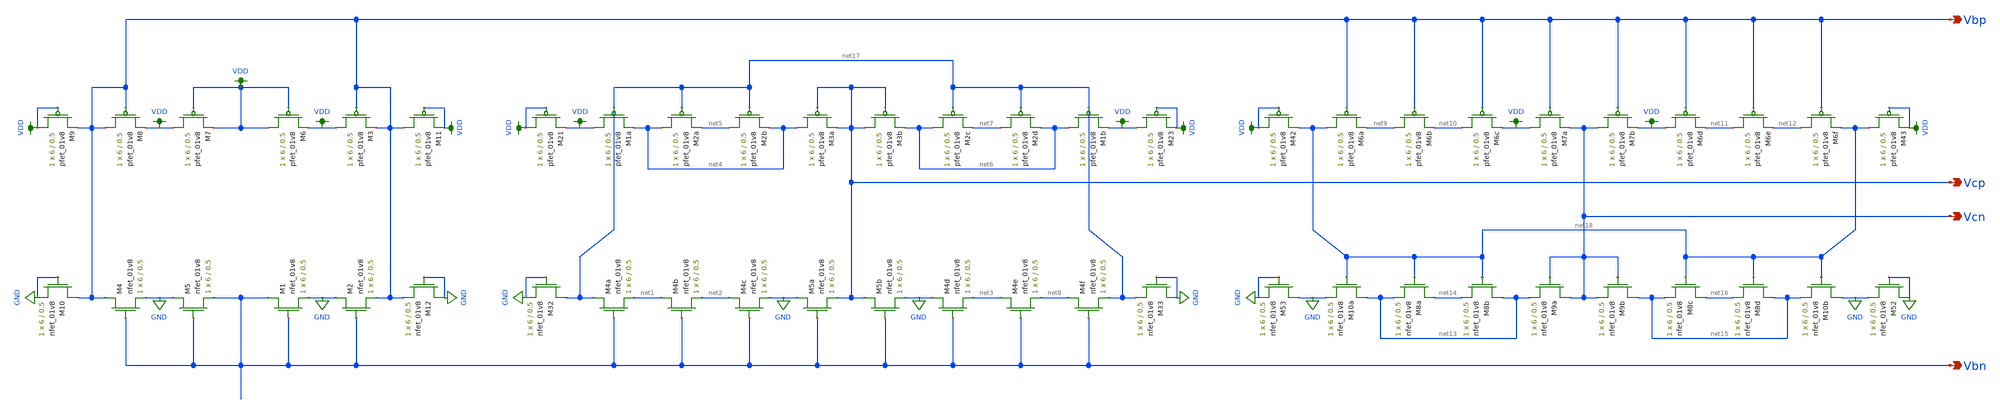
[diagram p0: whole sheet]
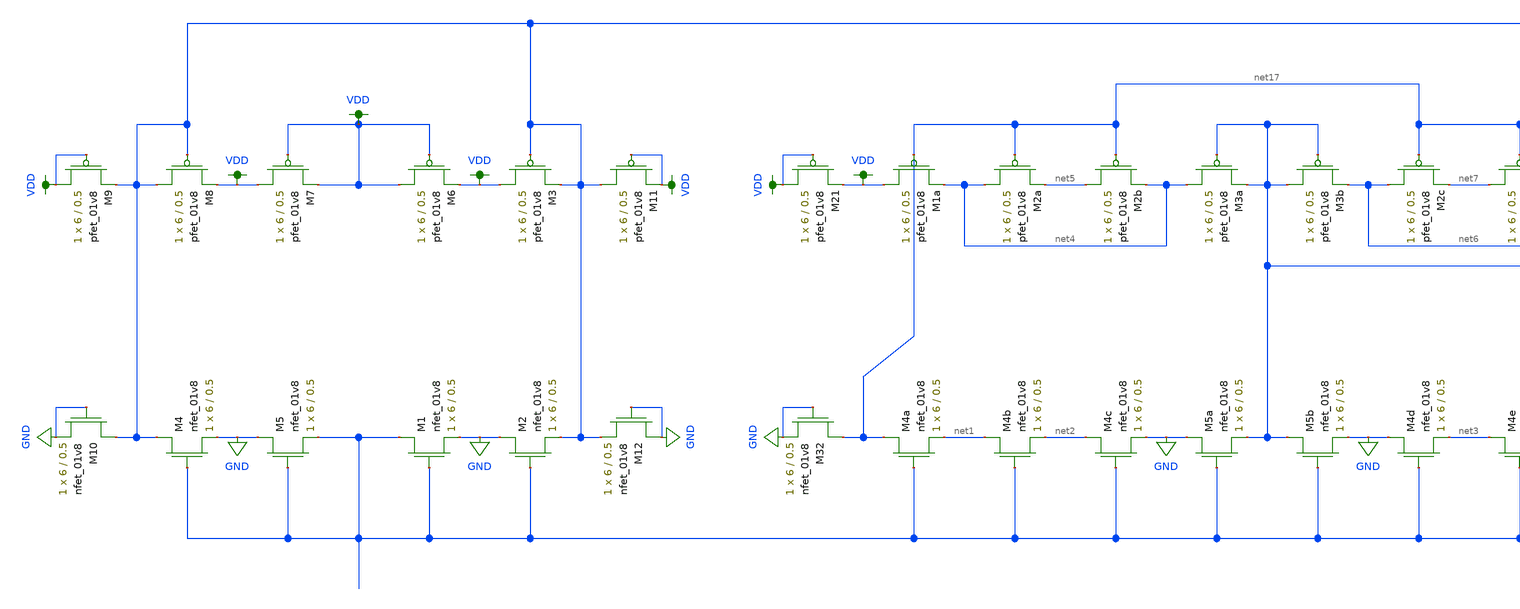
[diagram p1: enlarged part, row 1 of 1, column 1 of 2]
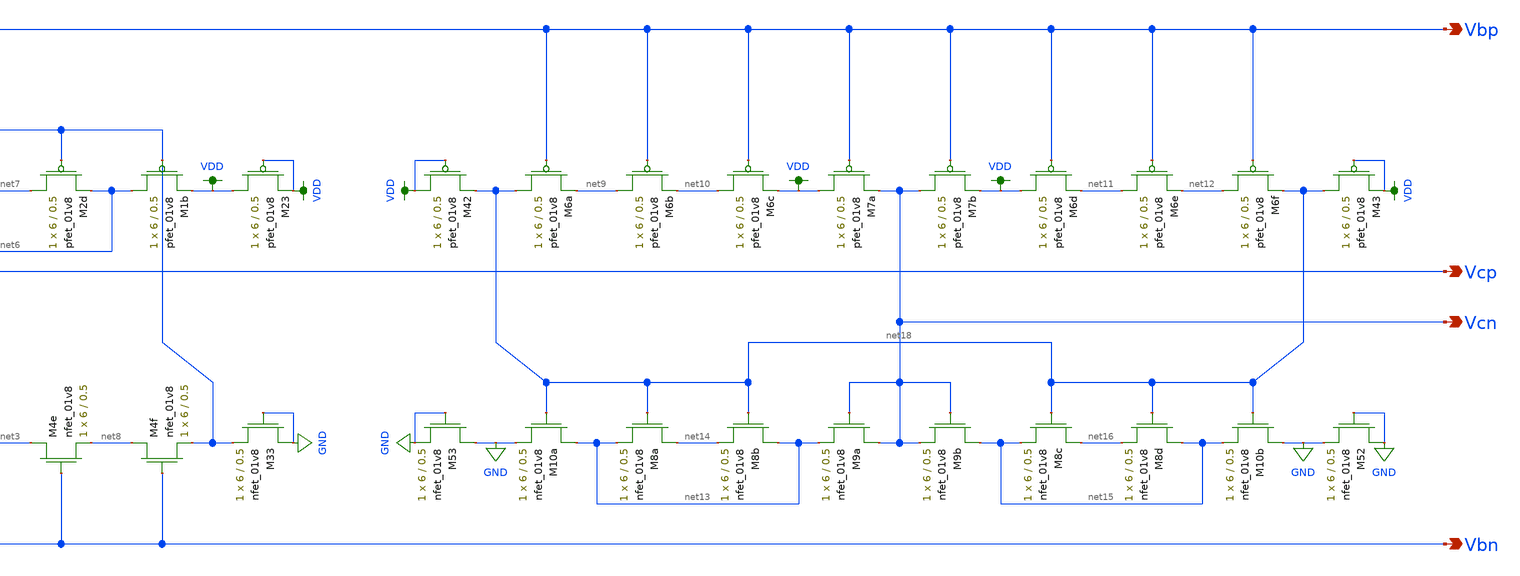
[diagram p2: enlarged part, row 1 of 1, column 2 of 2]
** sch_path: mini3/schem/bias_lvs.sch
**.subckt bias_lvs Vbn Vcn Vcp Vbp
*.opin Vbn
*.opin Vcn
*.opin Vcp
*.opin Vbp
XM4a net17 Vbn net1 GND sky130_fd_pr__nfet_01v8 L=0.5 W=6 nf=1 ad='int((nf+1)/2) * W/nf * 0.29' as='int((nf+2)/2) * W/nf * 0.29'
+ pd='2*int((nf+1)/2) * (W/nf + 0.29)' ps='2*int((nf+2)/2) * (W/nf + 0.29)' nrd='0.29 / W' nrs='0.29 / W'
+ sa=0 sb=0 sd=0 mult=1 m=1
XM4b net1 Vbn net2 GND sky130_fd_pr__nfet_01v8 L=0.5 W=6 nf=1 ad='int((nf+1)/2) * W/nf * 0.29' as='int((nf+2)/2) * W/nf * 0.29'
+ pd='2*int((nf+1)/2) * (W/nf + 0.29)' ps='2*int((nf+2)/2) * (W/nf + 0.29)' nrd='0.29 / W' nrs='0.29 / W'
+ sa=0 sb=0 sd=0 mult=1 m=1
XM4c net2 Vbn GND GND sky130_fd_pr__nfet_01v8 L=0.5 W=6 nf=1 ad='int((nf+1)/2) * W/nf * 0.29' as='int((nf+2)/2) * W/nf * 0.29'
+ pd='2*int((nf+1)/2) * (W/nf + 0.29)' ps='2*int((nf+2)/2) * (W/nf + 0.29)' nrd='0.29 / W' nrs='0.29 / W'
+ sa=0 sb=0 sd=0 mult=1 m=1
XM5a GND Vbn Vcp GND sky130_fd_pr__nfet_01v8 L=0.5 W=6 nf=1 ad='int((nf+1)/2) * W/nf * 0.29' as='int((nf+2)/2) * W/nf * 0.29'
+ pd='2*int((nf+1)/2) * (W/nf + 0.29)' ps='2*int((nf+2)/2) * (W/nf + 0.29)' nrd='0.29 / W' nrs='0.29 / W'
+ sa=0 sb=0 sd=0 mult=1 m=1
XM5b Vcp Vbn GND GND sky130_fd_pr__nfet_01v8 L=0.5 W=6 nf=1 ad='int((nf+1)/2) * W/nf * 0.29' as='int((nf+2)/2) * W/nf * 0.29'
+ pd='2*int((nf+1)/2) * (W/nf + 0.29)' ps='2*int((nf+2)/2) * (W/nf + 0.29)' nrd='0.29 / W' nrs='0.29 / W'
+ sa=0 sb=0 sd=0 mult=1 m=1
XM4d GND Vbn net3 GND sky130_fd_pr__nfet_01v8 L=0.5 W=6 nf=1 ad='int((nf+1)/2) * W/nf * 0.29' as='int((nf+2)/2) * W/nf * 0.29'
+ pd='2*int((nf+1)/2) * (W/nf + 0.29)' ps='2*int((nf+2)/2) * (W/nf + 0.29)' nrd='0.29 / W' nrs='0.29 / W'
+ sa=0 sb=0 sd=0 mult=1 m=1
XM4e net3 Vbn net8 GND sky130_fd_pr__nfet_01v8 L=0.5 W=6 nf=1 ad='int((nf+1)/2) * W/nf * 0.29' as='int((nf+2)/2) * W/nf * 0.29'
+ pd='2*int((nf+1)/2) * (W/nf + 0.29)' ps='2*int((nf+2)/2) * (W/nf + 0.29)' nrd='0.29 / W' nrs='0.29 / W'
+ sa=0 sb=0 sd=0 mult=1 m=1
XM4f net8 Vbn net17 GND sky130_fd_pr__nfet_01v8 L=0.5 W=6 nf=1 ad='int((nf+1)/2) * W/nf * 0.29' as='int((nf+2)/2) * W/nf * 0.29'
+ pd='2*int((nf+1)/2) * (W/nf + 0.29)' ps='2*int((nf+2)/2) * (W/nf + 0.29)' nrd='0.29 / W' nrs='0.29 / W'
+ sa=0 sb=0 sd=0 mult=1 m=1
XM1a VDD net17 net4 VDD sky130_fd_pr__pfet_01v8 L=0.5 W=6 nf=1 ad='int((nf+1)/2) * W/nf * 0.29' as='int((nf+2)/2) * W/nf * 0.29'
+ pd='2*int((nf+1)/2) * (W/nf + 0.29)' ps='2*int((nf+2)/2) * (W/nf + 0.29)' nrd='0.29 / W' nrs='0.29 / W'
+ sa=0 sb=0 sd=0 mult=1 m=1
XM2a net4 net17 net5 VDD sky130_fd_pr__pfet_01v8 L=0.5 W=6 nf=1 ad='int((nf+1)/2) * W/nf * 0.29' as='int((nf+2)/2) * W/nf * 0.29'
+ pd='2*int((nf+1)/2) * (W/nf + 0.29)' ps='2*int((nf+2)/2) * (W/nf + 0.29)' nrd='0.29 / W' nrs='0.29 / W'
+ sa=0 sb=0 sd=0 mult=1 m=1
XM2b net5 net17 net4 VDD sky130_fd_pr__pfet_01v8 L=0.5 W=6 nf=1 ad='int((nf+1)/2) * W/nf * 0.29' as='int((nf+2)/2) * W/nf * 0.29'
+ pd='2*int((nf+1)/2) * (W/nf + 0.29)' ps='2*int((nf+2)/2) * (W/nf + 0.29)' nrd='0.29 / W' nrs='0.29 / W'
+ sa=0 sb=0 sd=0 mult=1 m=1
XM3a net4 Vcp Vcp VDD sky130_fd_pr__pfet_01v8 L=0.5 W=6 nf=1 ad='int((nf+1)/2) * W/nf * 0.29' as='int((nf+2)/2) * W/nf * 0.29'
+ pd='2*int((nf+1)/2) * (W/nf + 0.29)' ps='2*int((nf+2)/2) * (W/nf + 0.29)' nrd='0.29 / W' nrs='0.29 / W'
+ sa=0 sb=0 sd=0 mult=1 m=1
XM3b Vcp Vcp net6 VDD sky130_fd_pr__pfet_01v8 L=0.5 W=6 nf=1 ad='int((nf+1)/2) * W/nf * 0.29' as='int((nf+2)/2) * W/nf * 0.29'
+ pd='2*int((nf+1)/2) * (W/nf + 0.29)' ps='2*int((nf+2)/2) * (W/nf + 0.29)' nrd='0.29 / W' nrs='0.29 / W'
+ sa=0 sb=0 sd=0 mult=1 m=1
XM2c net6 net17 net7 VDD sky130_fd_pr__pfet_01v8 L=0.5 W=6 nf=1 ad='int((nf+1)/2) * W/nf * 0.29' as='int((nf+2)/2) * W/nf * 0.29'
+ pd='2*int((nf+1)/2) * (W/nf + 0.29)' ps='2*int((nf+2)/2) * (W/nf + 0.29)' nrd='0.29 / W' nrs='0.29 / W'
+ sa=0 sb=0 sd=0 mult=1 m=1
XM2d net7 net17 net6 VDD sky130_fd_pr__pfet_01v8 L=0.5 W=6 nf=1 ad='int((nf+1)/2) * W/nf * 0.29' as='int((nf+2)/2) * W/nf * 0.29'
+ pd='2*int((nf+1)/2) * (W/nf + 0.29)' ps='2*int((nf+2)/2) * (W/nf + 0.29)' nrd='0.29 / W' nrs='0.29 / W'
+ sa=0 sb=0 sd=0 mult=1 m=1
XM1b net6 net17 VDD VDD sky130_fd_pr__pfet_01v8 L=0.5 W=6 nf=1 ad='int((nf+1)/2) * W/nf * 0.29' as='int((nf+2)/2) * W/nf * 0.29'
+ pd='2*int((nf+1)/2) * (W/nf + 0.29)' ps='2*int((nf+2)/2) * (W/nf + 0.29)' nrd='0.29 / W' nrs='0.29 / W'
+ sa=0 sb=0 sd=0 mult=1 m=1
XM6a net18 Vbp net9 VDD sky130_fd_pr__pfet_01v8 L=0.5 W=6 nf=1 ad='int((nf+1)/2) * W/nf * 0.29' as='int((nf+2)/2) * W/nf * 0.29'
+ pd='2*int((nf+1)/2) * (W/nf + 0.29)' ps='2*int((nf+2)/2) * (W/nf + 0.29)' nrd='0.29 / W' nrs='0.29 / W'
+ sa=0 sb=0 sd=0 mult=1 m=1
XM6b net9 Vbp net10 VDD sky130_fd_pr__pfet_01v8 L=0.5 W=6 nf=1 ad='int((nf+1)/2) * W/nf * 0.29' as='int((nf+2)/2) * W/nf * 0.29'
+ pd='2*int((nf+1)/2) * (W/nf + 0.29)' ps='2*int((nf+2)/2) * (W/nf + 0.29)' nrd='0.29 / W' nrs='0.29 / W'
+ sa=0 sb=0 sd=0 mult=1 m=1
XM6c net10 Vbp VDD VDD sky130_fd_pr__pfet_01v8 L=0.5 W=6 nf=1 ad='int((nf+1)/2) * W/nf * 0.29' as='int((nf+2)/2) * W/nf * 0.29'
+ pd='2*int((nf+1)/2) * (W/nf + 0.29)' ps='2*int((nf+2)/2) * (W/nf + 0.29)' nrd='0.29 / W' nrs='0.29 / W'
+ sa=0 sb=0 sd=0 mult=1 m=1
XM7a VDD Vbp Vcn VDD sky130_fd_pr__pfet_01v8 L=0.5 W=6 nf=1 ad='int((nf+1)/2) * W/nf * 0.29' as='int((nf+2)/2) * W/nf * 0.29'
+ pd='2*int((nf+1)/2) * (W/nf + 0.29)' ps='2*int((nf+2)/2) * (W/nf + 0.29)' nrd='0.29 / W' nrs='0.29 / W'
+ sa=0 sb=0 sd=0 mult=1 m=1
XM7b Vcn Vbp VDD VDD sky130_fd_pr__pfet_01v8 L=0.5 W=6 nf=1 ad='int((nf+1)/2) * W/nf * 0.29' as='int((nf+2)/2) * W/nf * 0.29'
+ pd='2*int((nf+1)/2) * (W/nf + 0.29)' ps='2*int((nf+2)/2) * (W/nf + 0.29)' nrd='0.29 / W' nrs='0.29 / W'
+ sa=0 sb=0 sd=0 mult=1 m=1
XM6d VDD Vbp net11 VDD sky130_fd_pr__pfet_01v8 L=0.5 W=6 nf=1 ad='int((nf+1)/2) * W/nf * 0.29' as='int((nf+2)/2) * W/nf * 0.29'
+ pd='2*int((nf+1)/2) * (W/nf + 0.29)' ps='2*int((nf+2)/2) * (W/nf + 0.29)' nrd='0.29 / W' nrs='0.29 / W'
+ sa=0 sb=0 sd=0 mult=1 m=1
XM6e net11 Vbp net12 VDD sky130_fd_pr__pfet_01v8 L=0.5 W=6 nf=1 ad='int((nf+1)/2) * W/nf * 0.29' as='int((nf+2)/2) * W/nf * 0.29'
+ pd='2*int((nf+1)/2) * (W/nf + 0.29)' ps='2*int((nf+2)/2) * (W/nf + 0.29)' nrd='0.29 / W' nrs='0.29 / W'
+ sa=0 sb=0 sd=0 mult=1 m=1
XM6f net12 Vbp net18 VDD sky130_fd_pr__pfet_01v8 L=0.5 W=6 nf=1 ad='int((nf+1)/2) * W/nf * 0.29' as='int((nf+2)/2) * W/nf * 0.29'
+ pd='2*int((nf+1)/2) * (W/nf + 0.29)' ps='2*int((nf+2)/2) * (W/nf + 0.29)' nrd='0.29 / W' nrs='0.29 / W'
+ sa=0 sb=0 sd=0 mult=1 m=1
XM10a net13 net18 GND GND sky130_fd_pr__nfet_01v8 L=0.5 W=6 nf=1 ad='int((nf+1)/2) * W/nf * 0.29' as='int((nf+2)/2) * W/nf * 0.29'
+ pd='2*int((nf+1)/2) * (W/nf + 0.29)' ps='2*int((nf+2)/2) * (W/nf + 0.29)' nrd='0.29 / W' nrs='0.29 / W'
+ sa=0 sb=0 sd=0 mult=1 m=1
XM8a net14 net18 net13 GND sky130_fd_pr__nfet_01v8 L=0.5 W=6 nf=1 ad='int((nf+1)/2) * W/nf * 0.29' as='int((nf+2)/2) * W/nf * 0.29'
+ pd='2*int((nf+1)/2) * (W/nf + 0.29)' ps='2*int((nf+2)/2) * (W/nf + 0.29)' nrd='0.29 / W' nrs='0.29 / W'
+ sa=0 sb=0 sd=0 mult=1 m=1
XM8b net13 net18 net14 GND sky130_fd_pr__nfet_01v8 L=0.5 W=6 nf=1 ad='int((nf+1)/2) * W/nf * 0.29' as='int((nf+2)/2) * W/nf * 0.29'
+ pd='2*int((nf+1)/2) * (W/nf + 0.29)' ps='2*int((nf+2)/2) * (W/nf + 0.29)' nrd='0.29 / W' nrs='0.29 / W'
+ sa=0 sb=0 sd=0 mult=1 m=1
XM9a Vcn Vcn net13 GND sky130_fd_pr__nfet_01v8 L=0.5 W=6 nf=1 ad='int((nf+1)/2) * W/nf * 0.29' as='int((nf+2)/2) * W/nf * 0.29'
+ pd='2*int((nf+1)/2) * (W/nf + 0.29)' ps='2*int((nf+2)/2) * (W/nf + 0.29)' nrd='0.29 / W' nrs='0.29 / W'
+ sa=0 sb=0 sd=0 mult=1 m=1
XM9b net15 Vcn Vcn GND sky130_fd_pr__nfet_01v8 L=0.5 W=6 nf=1 ad='int((nf+1)/2) * W/nf * 0.29' as='int((nf+2)/2) * W/nf * 0.29'
+ pd='2*int((nf+1)/2) * (W/nf + 0.29)' ps='2*int((nf+2)/2) * (W/nf + 0.29)' nrd='0.29 / W' nrs='0.29 / W'
+ sa=0 sb=0 sd=0 mult=1 m=1
XM8c net16 net18 net15 GND sky130_fd_pr__nfet_01v8 L=0.5 W=6 nf=1 ad='int((nf+1)/2) * W/nf * 0.29' as='int((nf+2)/2) * W/nf * 0.29'
+ pd='2*int((nf+1)/2) * (W/nf + 0.29)' ps='2*int((nf+2)/2) * (W/nf + 0.29)' nrd='0.29 / W' nrs='0.29 / W'
+ sa=0 sb=0 sd=0 mult=1 m=1
XM8d net15 net18 net16 GND sky130_fd_pr__nfet_01v8 L=0.5 W=6 nf=1 ad='int((nf+1)/2) * W/nf * 0.29' as='int((nf+2)/2) * W/nf * 0.29'
+ pd='2*int((nf+1)/2) * (W/nf + 0.29)' ps='2*int((nf+2)/2) * (W/nf + 0.29)' nrd='0.29 / W' nrs='0.29 / W'
+ sa=0 sb=0 sd=0 mult=1 m=1
XM10b GND net18 net15 GND sky130_fd_pr__nfet_01v8 L=0.5 W=6 nf=1 ad='int((nf+1)/2) * W/nf * 0.29' as='int((nf+2)/2) * W/nf * 0.29'
+ pd='2*int((nf+1)/2) * (W/nf + 0.29)' ps='2*int((nf+2)/2) * (W/nf + 0.29)' nrd='0.29 / W' nrs='0.29 / W'
+ sa=0 sb=0 sd=0 mult=1 m=1
XM23 VDD VDD VDD VDD sky130_fd_pr__pfet_01v8 L=0.5 W=6 nf=1 ad='int((nf+1)/2) * W/nf * 0.29' as='int((nf+2)/2) * W/nf * 0.29'
+ pd='2*int((nf+1)/2) * (W/nf + 0.29)' ps='2*int((nf+2)/2) * (W/nf + 0.29)' nrd='0.29 / W' nrs='0.29 / W'
+ sa=0 sb=0 sd=0 mult=1 m=1
XM32 net17 GND GND GND sky130_fd_pr__nfet_01v8 L=0.5 W=6 nf=1 ad='int((nf+1)/2) * W/nf * 0.29' as='int((nf+2)/2) * W/nf * 0.29'
+ pd='2*int((nf+1)/2) * (W/nf + 0.29)' ps='2*int((nf+2)/2) * (W/nf + 0.29)' nrd='0.29 / W' nrs='0.29 / W'
+ sa=0 sb=0 sd=0 mult=1 m=1
XM33 GND GND net17 GND sky130_fd_pr__nfet_01v8 L=0.5 W=6 nf=1 ad='int((nf+1)/2) * W/nf * 0.29' as='int((nf+2)/2) * W/nf * 0.29'
+ pd='2*int((nf+1)/2) * (W/nf + 0.29)' ps='2*int((nf+2)/2) * (W/nf + 0.29)' nrd='0.29 / W' nrs='0.29 / W'
+ sa=0 sb=0 sd=0 mult=1 m=1
XM42 VDD VDD net18 VDD sky130_fd_pr__pfet_01v8 L=0.5 W=6 nf=1 ad='int((nf+1)/2) * W/nf * 0.29' as='int((nf+2)/2) * W/nf * 0.29'
+ pd='2*int((nf+1)/2) * (W/nf + 0.29)' ps='2*int((nf+2)/2) * (W/nf + 0.29)' nrd='0.29 / W' nrs='0.29 / W'
+ sa=0 sb=0 sd=0 mult=1 m=1
XM43 net18 VDD VDD VDD sky130_fd_pr__pfet_01v8 L=0.5 W=6 nf=1 ad='int((nf+1)/2) * W/nf * 0.29' as='int((nf+2)/2) * W/nf * 0.29'
+ pd='2*int((nf+1)/2) * (W/nf + 0.29)' ps='2*int((nf+2)/2) * (W/nf + 0.29)' nrd='0.29 / W' nrs='0.29 / W'
+ sa=0 sb=0 sd=0 mult=1 m=1
XM52 GND GND GND GND sky130_fd_pr__nfet_01v8 L=0.5 W=6 nf=1 ad='int((nf+1)/2) * W/nf * 0.29' as='int((nf+2)/2) * W/nf * 0.29'
+ pd='2*int((nf+1)/2) * (W/nf + 0.29)' ps='2*int((nf+2)/2) * (W/nf + 0.29)' nrd='0.29 / W' nrs='0.29 / W'
+ sa=0 sb=0 sd=0 mult=1 m=1
XM53 GND GND GND GND sky130_fd_pr__nfet_01v8 L=0.5 W=6 nf=1 ad='int((nf+1)/2) * W/nf * 0.29' as='int((nf+2)/2) * W/nf * 0.29'
+ pd='2*int((nf+1)/2) * (W/nf + 0.29)' ps='2*int((nf+2)/2) * (W/nf + 0.29)' nrd='0.29 / W' nrs='0.29 / W'
+ sa=0 sb=0 sd=0 mult=1 m=1
XM21 VDD VDD VDD VDD sky130_fd_pr__pfet_01v8 L=0.5 W=6 nf=1 ad='int((nf+1)/2) * W/nf * 0.29' as='int((nf+2)/2) * W/nf * 0.29'
+ pd='2*int((nf+1)/2) * (W/nf + 0.29)' ps='2*int((nf+2)/2) * (W/nf + 0.29)' nrd='0.29 / W' nrs='0.29 / W'
+ sa=0 sb=0 sd=0 mult=1 m=1
XM1 Vbn Vbn GND GND sky130_fd_pr__nfet_01v8 L=0.5 W=6 nf=1 ad='int((nf+1)/2) * W/nf * 0.29' as='int((nf+2)/2) * W/nf * 0.29'
+ pd='2*int((nf+1)/2) * (W/nf + 0.29)' ps='2*int((nf+2)/2) * (W/nf + 0.29)' nrd='0.29 / W' nrs='0.29 / W'
+ sa=0 sb=0 sd=0 mult=1 m=1
XM2 GND Vbn Vbp GND sky130_fd_pr__nfet_01v8 L=0.5 W=6 nf=1 ad='int((nf+1)/2) * W/nf * 0.29' as='int((nf+2)/2) * W/nf * 0.29'
+ pd='2*int((nf+1)/2) * (W/nf + 0.29)' ps='2*int((nf+2)/2) * (W/nf + 0.29)' nrd='0.29 / W' nrs='0.29 / W'
+ sa=0 sb=0 sd=0 mult=1 m=1
XM3 VDD Vbp Vbp VDD sky130_fd_pr__pfet_01v8 L=0.5 W=6 nf=1 ad='int((nf+1)/2) * W/nf * 0.29' as='int((nf+2)/2) * W/nf * 0.29'
+ pd='2*int((nf+1)/2) * (W/nf + 0.29)' ps='2*int((nf+2)/2) * (W/nf + 0.29)' nrd='0.29 / W' nrs='0.29 / W'
+ sa=0 sb=0 sd=0 mult=1 m=1
XM4 Vbp Vbn GND GND sky130_fd_pr__nfet_01v8 L=0.5 W=6 nf=1 ad='int((nf+1)/2) * W/nf * 0.29' as='int((nf+2)/2) * W/nf * 0.29'
+ pd='2*int((nf+1)/2) * (W/nf + 0.29)' ps='2*int((nf+2)/2) * (W/nf + 0.29)' nrd='0.29 / W' nrs='0.29 / W'
+ sa=0 sb=0 sd=0 mult=1 m=1
XM5 GND Vbn Vbn GND sky130_fd_pr__nfet_01v8 L=0.5 W=6 nf=1 ad='int((nf+1)/2) * W/nf * 0.29' as='int((nf+2)/2) * W/nf * 0.29'
+ pd='2*int((nf+1)/2) * (W/nf + 0.29)' ps='2*int((nf+2)/2) * (W/nf + 0.29)' nrd='0.29 / W' nrs='0.29 / W'
+ sa=0 sb=0 sd=0 mult=1 m=1
XM6 VDD VDD VDD VDD sky130_fd_pr__pfet_01v8 L=0.5 W=6 nf=1 ad='int((nf+1)/2) * W/nf * 0.29' as='int((nf+2)/2) * W/nf * 0.29'
+ pd='2*int((nf+1)/2) * (W/nf + 0.29)' ps='2*int((nf+2)/2) * (W/nf + 0.29)' nrd='0.29 / W' nrs='0.29 / W'
+ sa=0 sb=0 sd=0 mult=1 m=1
XM7 VDD VDD VDD VDD sky130_fd_pr__pfet_01v8 L=0.5 W=6 nf=1 ad='int((nf+1)/2) * W/nf * 0.29' as='int((nf+2)/2) * W/nf * 0.29'
+ pd='2*int((nf+1)/2) * (W/nf + 0.29)' ps='2*int((nf+2)/2) * (W/nf + 0.29)' nrd='0.29 / W' nrs='0.29 / W'
+ sa=0 sb=0 sd=0 mult=1 m=1
XM8 Vbp Vbp VDD VDD sky130_fd_pr__pfet_01v8 L=0.5 W=6 nf=1 ad='int((nf+1)/2) * W/nf * 0.29' as='int((nf+2)/2) * W/nf * 0.29'
+ pd='2*int((nf+1)/2) * (W/nf + 0.29)' ps='2*int((nf+2)/2) * (W/nf + 0.29)' nrd='0.29 / W' nrs='0.29 / W'
+ sa=0 sb=0 sd=0 mult=1 m=1
XM9 VDD VDD Vbp VDD sky130_fd_pr__pfet_01v8 L=0.5 W=6 nf=1 ad='int((nf+1)/2) * W/nf * 0.29' as='int((nf+2)/2) * W/nf * 0.29'
+ pd='2*int((nf+1)/2) * (W/nf + 0.29)' ps='2*int((nf+2)/2) * (W/nf + 0.29)' nrd='0.29 / W' nrs='0.29 / W'
+ sa=0 sb=0 sd=0 mult=1 m=1
XM10 Vbp GND GND GND sky130_fd_pr__nfet_01v8 L=0.5 W=6 nf=1 ad='int((nf+1)/2) * W/nf * 0.29' as='int((nf+2)/2) * W/nf * 0.29'
+ pd='2*int((nf+1)/2) * (W/nf + 0.29)' ps='2*int((nf+2)/2) * (W/nf + 0.29)' nrd='0.29 / W' nrs='0.29 / W'
+ sa=0 sb=0 sd=0 mult=1 m=1
XM11 Vbp VDD VDD VDD sky130_fd_pr__pfet_01v8 L=0.5 W=6 nf=1 ad='int((nf+1)/2) * W/nf * 0.29' as='int((nf+2)/2) * W/nf * 0.29'
+ pd='2*int((nf+1)/2) * (W/nf + 0.29)' ps='2*int((nf+2)/2) * (W/nf + 0.29)' nrd='0.29 / W' nrs='0.29 / W'
+ sa=0 sb=0 sd=0 mult=1 m=1
XM12 GND GND Vbp GND sky130_fd_pr__nfet_01v8 L=0.5 W=6 nf=1 ad='int((nf+1)/2) * W/nf * 0.29' as='int((nf+2)/2) * W/nf * 0.29'
+ pd='2*int((nf+1)/2) * (W/nf + 0.29)' ps='2*int((nf+2)/2) * (W/nf + 0.29)' nrd='0.29 / W' nrs='0.29 / W'
+ sa=0 sb=0 sd=0 mult=1 m=1
**.ends
.GLOBAL VDD
.GLOBAL GND
.end
